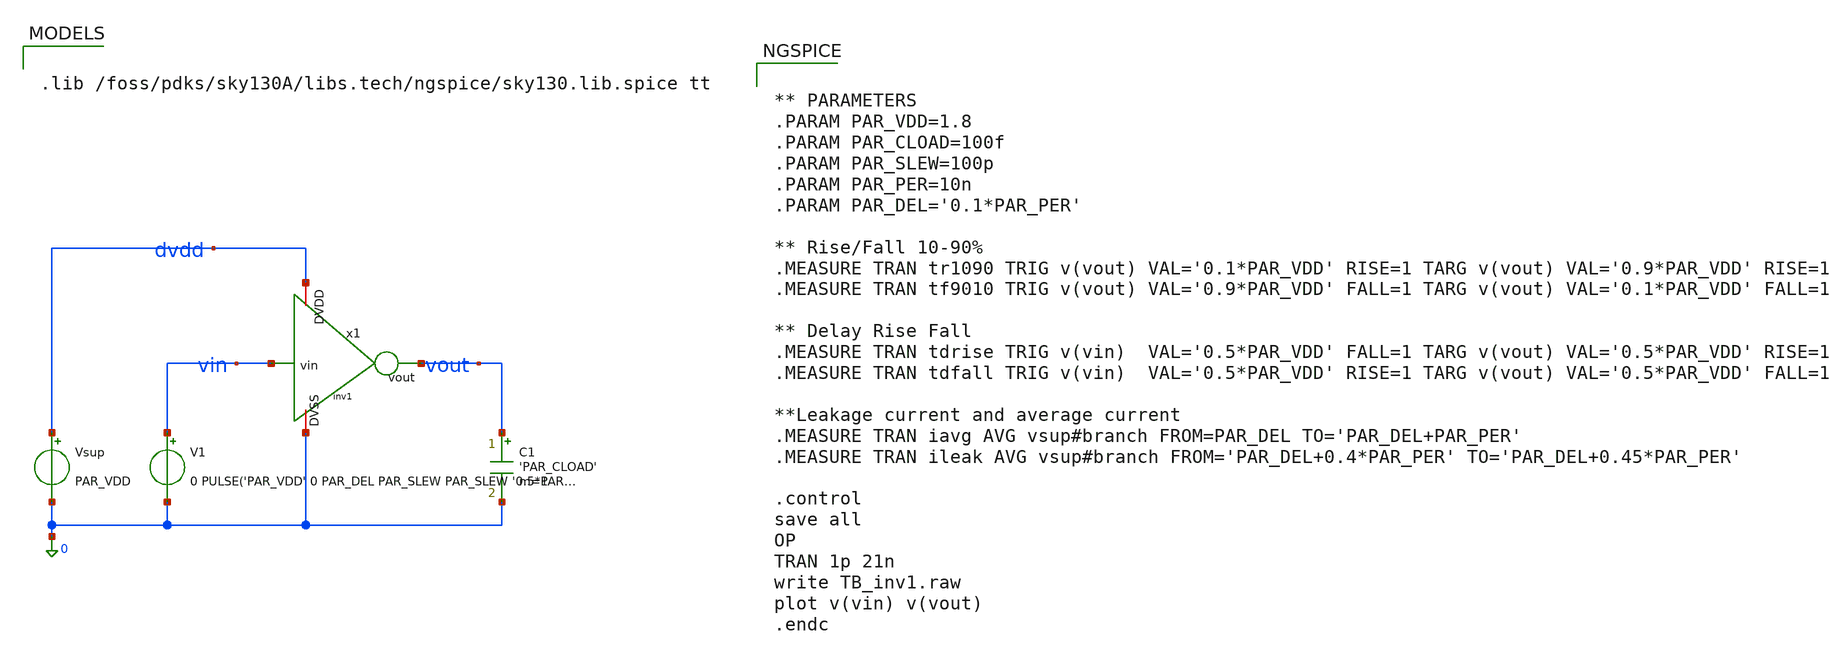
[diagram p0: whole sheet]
** sch_path: xschem/inverter/TB_inv1.sch
**.subckt TB_inv1
x1 dvdd vin vout 0 inv1
V1 vin 0 0 PULSE('PAR_VDD' 0 PAR_DEL PAR_SLEW PAR_SLEW '0.5*PAR_PER' '1.0*PAR_PER')
Vsup dvdd 0 PAR_VDD
C1 vout 0 'PAR_CLOAD' m=1
**** begin user architecture code


.lib /foss/pdks/sky130A/libs.tech/ngspice/sky130.lib.spice tt




** PARAMETERS
.PARAM PAR_VDD=1.8
.PARAM PAR_CLOAD=100f
.PARAM PAR_SLEW=100p
.PARAM PAR_PER=10n
.PARAM PAR_DEL='0.1*PAR_PER'

** Rise/Fall 10-90%
.MEASURE TRAN tr1090 TRIG v(vout) VAL='0.1*PAR_VDD' RISE=1 TARG v(vout) VAL='0.9*PAR_VDD' RISE=1
.MEASURE TRAN tf9010 TRIG v(vout) VAL='0.9*PAR_VDD' FALL=1 TARG v(vout) VAL='0.1*PAR_VDD' FALL=1

** Delay Rise Fall
.MEASURE TRAN tdrise TRIG v(vin)  VAL='0.5*PAR_VDD' FALL=1 TARG v(vout) VAL='0.5*PAR_VDD' RISE=1
.MEASURE TRAN tdfall TRIG v(vin)  VAL='0.5*PAR_VDD' RISE=1 TARG v(vout) VAL='0.5*PAR_VDD' FALL=1

**Leakage current and average current
.MEASURE TRAN iavg AVG vsup#branch FROM=PAR_DEL TO='PAR_DEL+PAR_PER'
.MEASURE TRAN ileak AVG vsup#branch FROM='PAR_DEL+0.4*PAR_PER' TO='PAR_DEL+0.45*PAR_PER'

.control
save all
OP
TRAN 1p 21n
write TB_inv1.raw
plot v(vin) v(vout)
.endc



**** end user architecture code
**.ends

* expanding   symbol:  /foss/designs/bos-sram-sky130/xschem/inverter/inv1.sym # of pins=4
** sym_path: /foss/designs/bos-sram-sky130/xschem/inverter/inv1.sym
** sch_path: /foss/designs/bos-sram-sky130/xschem/inverter/inv1.sch
.subckt inv1 DVDD vin vout DVSS
*.ipin vin
*.opin vout
*.iopin DVDD
*.iopin DVSS
XM1 vout vin DVDD DVDD sky130_fd_pr__pfet_01v8 L=0.15 W=2 nf=1 ad='int((nf+1)/2) * W/nf * 0.29' as='int((nf+2)/2) * W/nf * 0.29'
+ pd='2*int((nf+1)/2) * (W/nf + 0.29)' ps='2*int((nf+2)/2) * (W/nf + 0.29)' nrd='0.29 / W' nrs='0.29 / W'
+ sa=0 sb=0 sd=0 mult=1 m=1
XM2 vout vin DVSS DVSS sky130_fd_pr__nfet_01v8 L=0.15 W=1 nf=1 ad='int((nf+1)/2) * W/nf * 0.29' as='int((nf+2)/2) * W/nf * 0.29'
+ pd='2*int((nf+1)/2) * (W/nf + 0.29)' ps='2*int((nf+2)/2) * (W/nf + 0.29)' nrd='0.29 / W' nrs='0.29 / W'
+ sa=0 sb=0 sd=0 mult=1 m=1
.ends

.end
